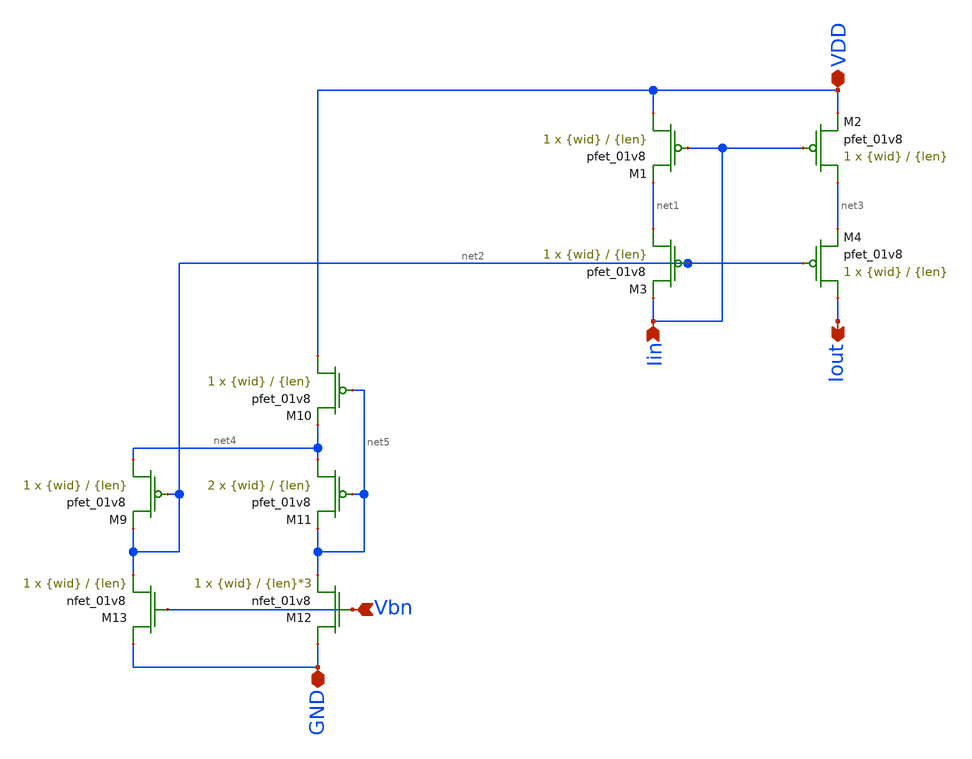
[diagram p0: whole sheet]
** sch_path: mp3/mirror_v2.sch
**.subckt mirror_v2 Vbn Iin GND VDD Iout
*.ipin Vbn
*.ipin Iin
*.iopin GND
*.iopin VDD
*.opin Iout
XM1 VDD Iin net1 VDD sky130_fd_pr__pfet_01v8 L={len} W={wid} nf=1 ad='int((nf+1)/2) * W/nf * 0.29' as='int((nf+2)/2) * W/nf * 0.29'
+ pd='2*int((nf+1)/2) * (W/nf + 0.29)' ps='2*int((nf+2)/2) * (W/nf + 0.29)' nrd='0.29 / W' nrs='0.29 / W'
+ sa=0 sb=0 sd=0 mult=1 m=1
XM2 net3 Iin VDD VDD sky130_fd_pr__pfet_01v8 L={len} W={wid} nf=1 ad='int((nf+1)/2) * W/nf * 0.29' as='int((nf+2)/2) * W/nf * 0.29'
+ pd='2*int((nf+1)/2) * (W/nf + 0.29)' ps='2*int((nf+2)/2) * (W/nf + 0.29)' nrd='0.29 / W' nrs='0.29 / W'
+ sa=0 sb=0 sd=0 mult=1 m=1
XM3 net1 net2 Iin VDD sky130_fd_pr__pfet_01v8 L={len} W={wid} nf=1 ad='int((nf+1)/2) * W/nf * 0.29' as='int((nf+2)/2) * W/nf * 0.29'
+ pd='2*int((nf+1)/2) * (W/nf + 0.29)' ps='2*int((nf+2)/2) * (W/nf + 0.29)' nrd='0.29 / W' nrs='0.29 / W'
+ sa=0 sb=0 sd=0 mult=1 m=1
XM4 Iout net2 net3 VDD sky130_fd_pr__pfet_01v8 L={len} W={wid} nf=1 ad='int((nf+1)/2) * W/nf * 0.29'
+ as='int((nf+2)/2) * W/nf * 0.29' pd='2*int((nf+1)/2) * (W/nf + 0.29)' ps='2*int((nf+2)/2) * (W/nf + 0.29)'
+ nrd='0.29 / W' nrs='0.29 / W' sa=0 sb=0 sd=0 mult=1 m=1
XM9 net4 net2 net2 VDD sky130_fd_pr__pfet_01v8 L={len} W={wid} nf=1 ad='int((nf+1)/2) * W/nf * 0.29'
+ as='int((nf+2)/2) * W/nf * 0.29' pd='2*int((nf+1)/2) * (W/nf + 0.29)' ps='2*int((nf+2)/2) * (W/nf + 0.29)'
+ nrd='0.29 / W' nrs='0.29 / W' sa=0 sb=0 sd=0 mult=1 m=1
XM10 VDD net5 net4 VDD sky130_fd_pr__pfet_01v8 L={len} W={wid} nf=1 ad='int((nf+1)/2) * W/nf * 0.29'
+ as='int((nf+2)/2) * W/nf * 0.29' pd='2*int((nf+1)/2) * (W/nf + 0.29)' ps='2*int((nf+2)/2) * (W/nf + 0.29)'
+ nrd='0.29 / W' nrs='0.29 / W' sa=0 sb=0 sd=0 mult=1 m=1
XM11 net4 net5 net5 VDD sky130_fd_pr__pfet_01v8 L={len} W={wid} nf=1 ad='int((nf+1)/2) * W/nf * 0.29'
+ as='int((nf+2)/2) * W/nf * 0.29' pd='2*int((nf+1)/2) * (W/nf + 0.29)' ps='2*int((nf+2)/2) * (W/nf + 0.29)'
+ nrd='0.29 / W' nrs='0.29 / W' sa=0 sb=0 sd=0 mult=2 m=2
XM12 GND Vbn net5 GND sky130_fd_pr__nfet_01v8 L={len}*3 W={wid} nf=1 ad='int((nf+1)/2) * W/nf * 0.29'
+ as='int((nf+2)/2) * W/nf * 0.29' pd='2*int((nf+1)/2) * (W/nf + 0.29)' ps='2*int((nf+2)/2) * (W/nf + 0.29)'
+ nrd='0.29 / W' nrs='0.29 / W' sa=0 sb=0 sd=0 mult=1 m=1
XM13 GND Vbn net2 GND sky130_fd_pr__nfet_01v8 L={len} W={wid} nf=1 ad='int((nf+1)/2) * W/nf * 0.29' as='int((nf+2)/2) * W/nf * 0.29'
+ pd='2*int((nf+1)/2) * (W/nf + 0.29)' ps='2*int((nf+2)/2) * (W/nf + 0.29)' nrd='0.29 / W' nrs='0.29 / W'
+ sa=0 sb=0 sd=0 mult=1 m=1
**.ends
.end
